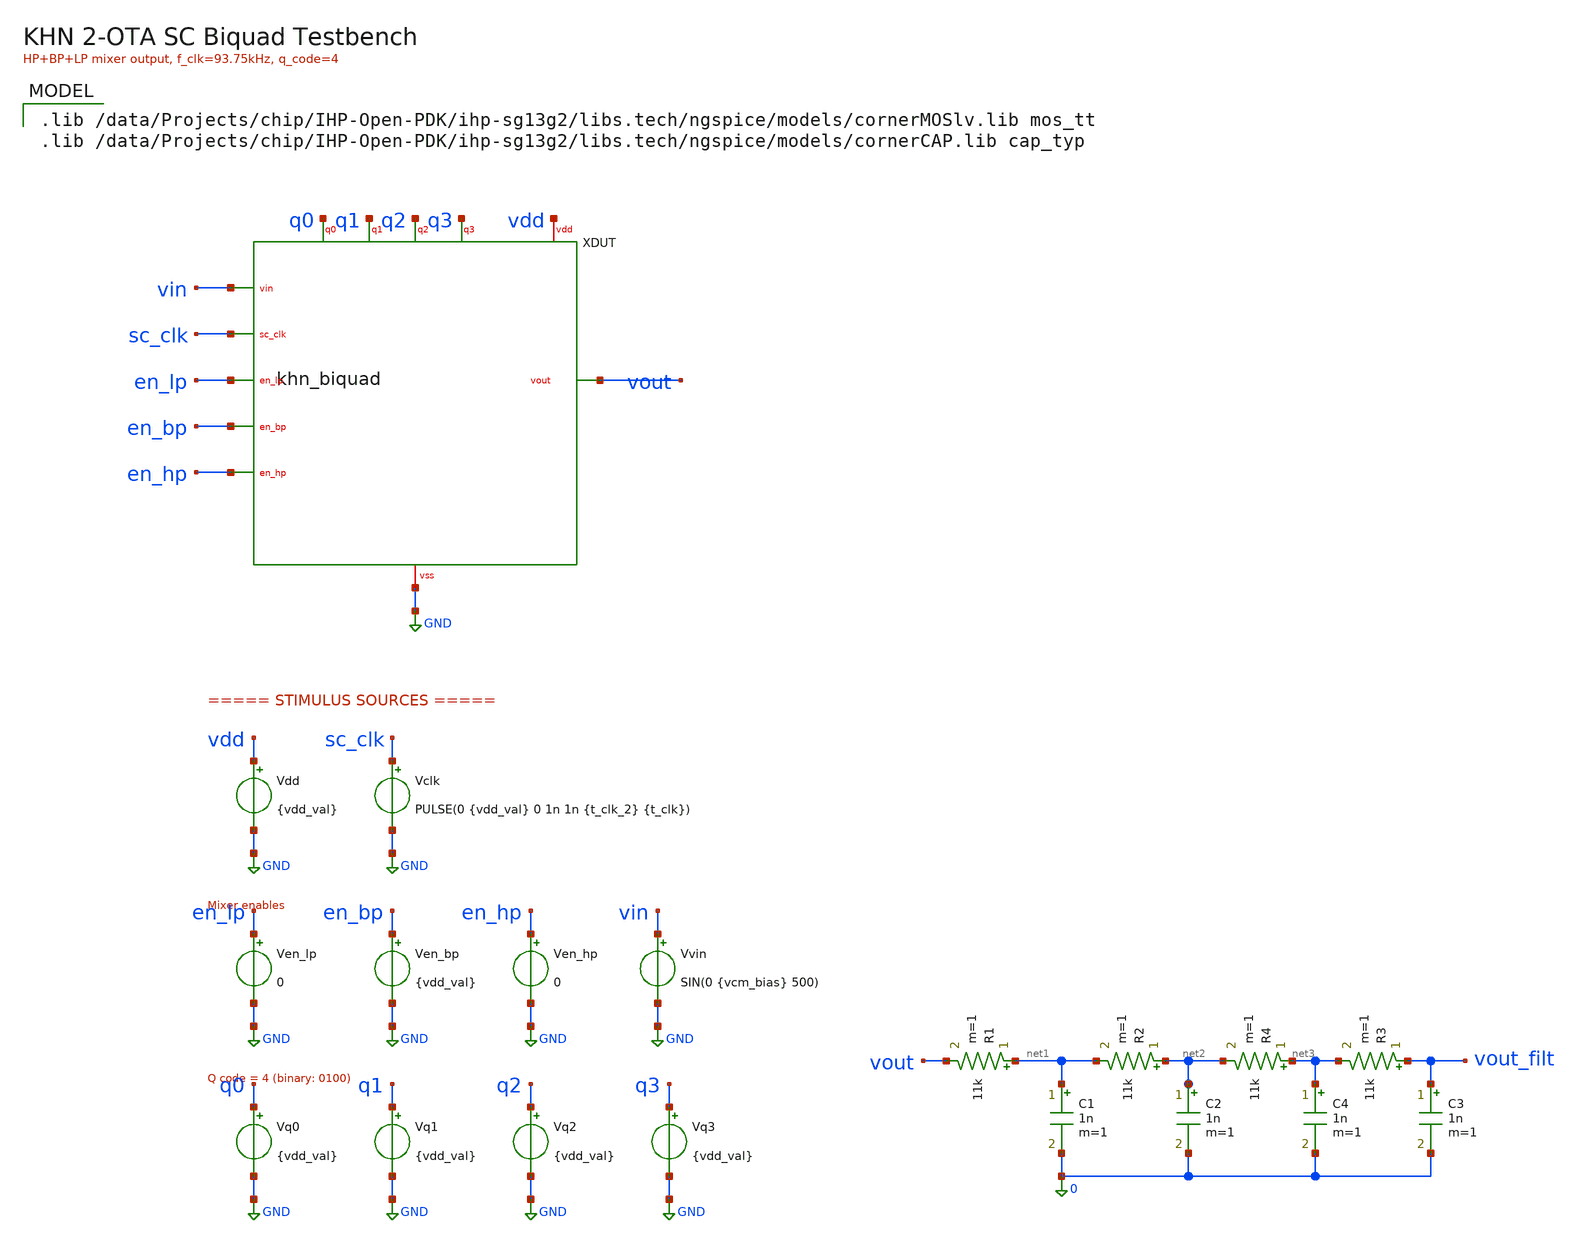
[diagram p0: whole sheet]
** sch_path: xschem/khn_biquad_nl.sch
**.subckt khn_biquad_nl
XDUT vin vout en_lp en_bp en_hp sc_clk q0 q1 q2 q3 vdd GND khn_biquad
Vdd vdd GND {vdd_val}
Vclk sc_clk GND PULSE(0 {vdd_val} 0 1n 1n {t_clk_2} {t_clk})
Vvin vin GND SIN(0 {vcm_bias} 500)
Ven_lp en_lp GND 0
Ven_bp en_bp GND {vdd_val}
Ven_hp en_hp GND 0
Vq0 q0 GND {vdd_val}
Vq1 q1 GND {vdd_val}
Vq2 q2 GND {vdd_val}
Vq3 q3 GND {vdd_val}
C1 net1 0 1n m=1
R1 net1 vout 11k m=1
R2 net2 net1 11k m=1
C2 net2 0 1n m=1
C3 vout_filt 0 1n m=1
R3 vout_filt net3 11k m=1
C4 net3 0 1n m=1
R4 net3 net2 11k m=1
**** begin user architecture code
 .lib /data/Projects/chip/IHP-Open-PDK/ihp-sg13g2/libs.tech/ngspice/models/cornerMOSlv.lib mos_tt
.lib /data/Projects/chip/IHP-Open-PDK/ihp-sg13g2/libs.tech/ngspice/models/cornerCAP.lib cap_typ



.options method=gear reltol=5e-3 abstol=1e-12 vntol=1e-6 gmin=1e-12
.param vdd_val = 1.2
.param f_clk = 13750
.param t_clk = {1/f_clk}
.param t_clk_2 = {t_clk/2 -1n}
.param vcm_bias = 0.47

* Force vcm to ideal voltage for SC debugging (bypasses weak bias gen)
Vvcm xdut.vcm 0 {vcm_bias}

* SC nodes float during DC OP — initialize near VCM and let transient settle
.ic v(xdut.bp)=0.614 v(xdut.lp)=0.614 v(xdut.hp)=0.47  v(xdut.sum1)=0.47 v(xdut.sum2)=0.47
+ v(xdut.sum3)=0.47  v(xdut.vcm)=0.47  v(xdut.cin_t)=0.47 v(xdut.cin_b)=0.47  v(xdut.cfb_t)=0.47 v(xdut.cfb_b)=0.47
+  v(xdut.cis_t)=0.47 v(xdut.cis_b)=0.47  v(xdut.c5_t)=0.47 v(xdut.c5_b)=0.47  v(xdut.c6_t)=0.47 v(xdut.c6_b)=0.47
+  v(xdut.cq0_t)=0.47 v(xdut.cq1_t)=0.47 v(xdut.cq2_t)=0.47 v(xdut.cq3_t)=0.47  v(xdut.x_ota1.mirr)=0.72
+ v(xdut.x_ota1.tail)=0.12  v(xdut.x_ota2.mirr)=0.72 v(xdut.x_ota2.tail)=0.12  v(xdut.x_ota3.mirr)=0.72
+ v(xdut.x_ota3.tail)=0.12  v(xdut.phi1)=0 v(xdut.n1)=1.2 v(xdut.n3)=1.2


.tran {t_clk/20} {800*t_clk} UIC
.control

  let start_freq = 10k
  let stop_freq = 260k
  let delta_freq = 50k
  let freq_act = start_freq

  * loop
  while freq_act le stop_freq
    *
    *reset
    *run
    let t_clk_new = {1/freq_act}
    let t_clk_2_new = {t_clk_new/2-1n}
    alterparam t_clk = $&t_clk_new
    alterparam t_clk_2 = $&t_clk_2_new

    print t_clk_2_new
    print t_clk_new

    *let f_clk = freq_act
    *let t_clk = {1/f_clk}
    *let t_clk_2 = {{t_clk/2}-1n}

    *print f_clk
    *print t_clk
    *print t_clk_2

    *alter @Vclk[PULSE] = [ 0 {vdd_val/2} 0 1n 1n $&t_clk_2 $&t_clk ]
    reset
    run
    write khn_biquad.out v(vout)
    write khn_biquad_tb.raw v(vin) v(vout) v(xdut.bp) v(xdut.lp) v(xdut.hp) v(xdut.sum1)
+ v(xdut.sum2) v(xdut.sum3)
    set wr_singlescale
    wrdata khn_biquad_tran.data v(vout) v(xdut.bp) v(xdut.lp) v(xdut.hp) v(xdut.vcm)
    let freq_act = freq_act + delta_freq


  end
  plot tran1.vout_filt tran2.vout_filt tran3.vout_filt tran4.vout_filt tran5.vout_filt
.endc


**** end user architecture code
**.ends

* expanding   symbol:  khn_biquad.sym # of pins=12
** sym_path: xschem/khn_biquad.sym
/data/Projects/tiny_workspace/macros/gds/khn_biquad_extracted.cir
.GLOBAL GND
.end
